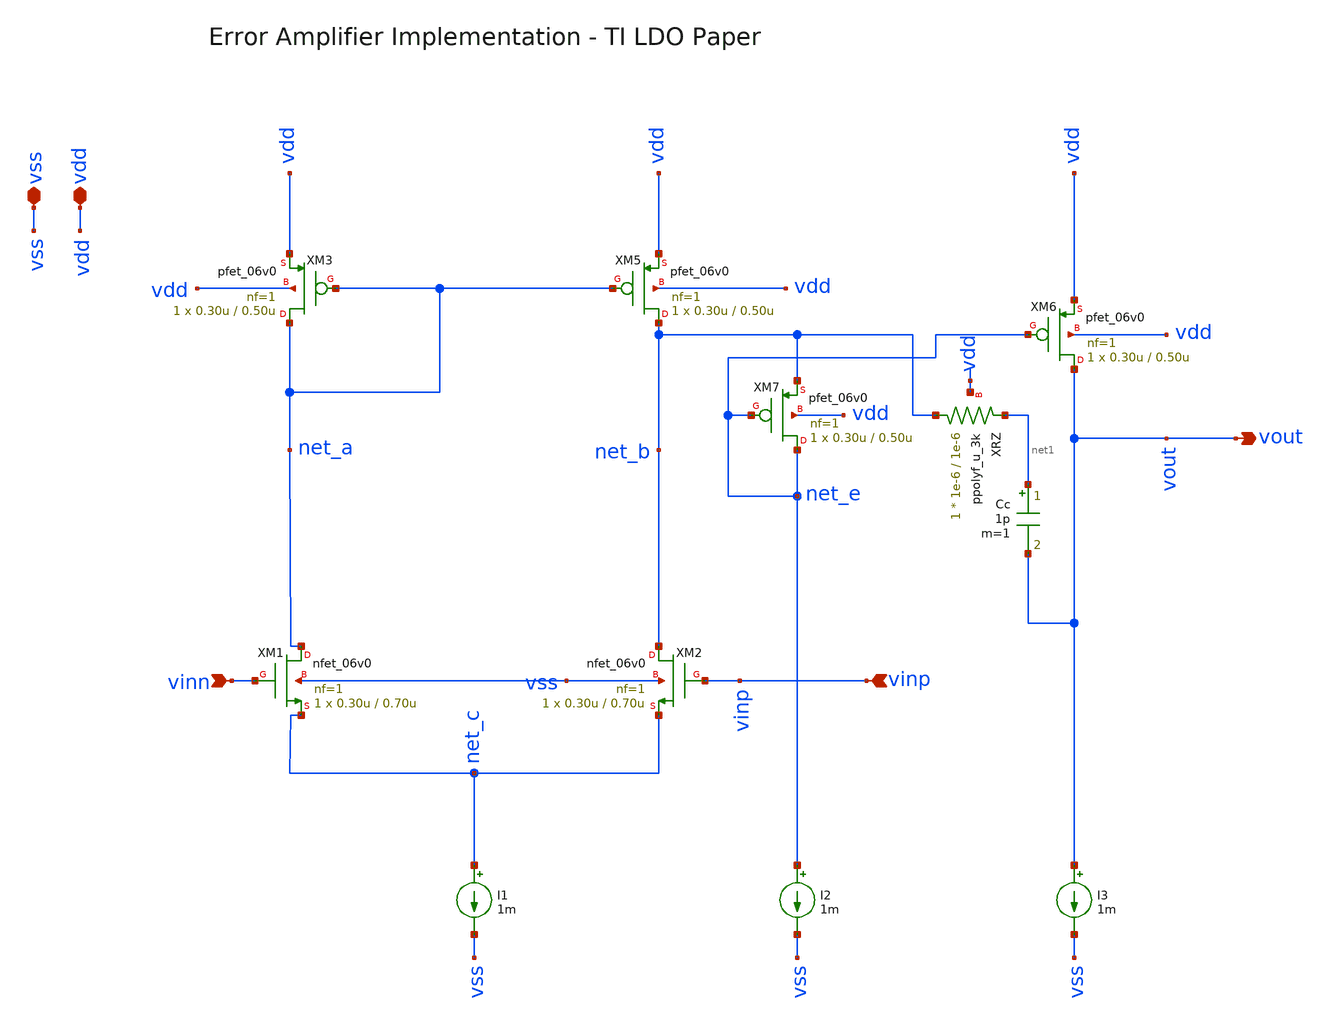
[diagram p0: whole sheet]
** sch_path: analog-db/drawings/ldo-005-ti-ldo-buffer-ref/gf180/error_amp/error_amp_diode_connected.sch
**.subckt error_amp_diode_connected vdd vss vinp vout vinn
*.iopin vdd
*.iopin vss
*.ipin vinp
*.opin vout
*.ipin vinn
XM2 net_b vinp net_c vss nfet_06v0 L=0.70u W=0.30u nf=1 ad='int((nf+1)/2) * W/nf * 0.18u' as='int((nf+2)/2) * W/nf * 0.18u'
+ pd='2*int((nf+1)/2) * (W/nf + 0.18u)' ps='2*int((nf+2)/2) * (W/nf + 0.18u)' nrd='0.18u / W' nrs='0.18u / W'
+ sa=0 sb=0 sd=0 m=1
I1 net_c vss 1m
I2 net_e vss 1m
I3 vout vss 1m
XM3 net_a net_a vdd vdd pfet_06v0 L=0.50u W=0.30u nf=1 ad='int((nf+1)/2) * W/nf * 0.18u' as='int((nf+2)/2) * W/nf * 0.18u'
+ pd='2*int((nf+1)/2) * (W/nf + 0.18u)' ps='2*int((nf+2)/2) * (W/nf + 0.18u)' nrd='0.18u / W' nrs='0.18u / W'
+ sa=0 sb=0 sd=0 m=1
XM5 net_b net_a vdd vdd pfet_06v0 L=0.50u W=0.30u nf=1 ad='int((nf+1)/2) * W/nf * 0.18u' as='int((nf+2)/2) * W/nf * 0.18u'
+ pd='2*int((nf+1)/2) * (W/nf + 0.18u)' ps='2*int((nf+2)/2) * (W/nf + 0.18u)' nrd='0.18u / W' nrs='0.18u / W'
+ sa=0 sb=0 sd=0 m=1
XM6 vout net_e vdd vdd pfet_06v0 L=0.50u W=0.30u nf=1 ad='int((nf+1)/2) * W/nf * 0.18u' as='int((nf+2)/2) * W/nf * 0.18u'
+ pd='2*int((nf+1)/2) * (W/nf + 0.18u)' ps='2*int((nf+2)/2) * (W/nf + 0.18u)' nrd='0.18u / W' nrs='0.18u / W'
+ sa=0 sb=0 sd=0 m=1
XM7 net_e net_e net_b vdd pfet_06v0 L=0.50u W=0.30u nf=1 ad='int((nf+1)/2) * W/nf * 0.18u' as='int((nf+2)/2) * W/nf * 0.18u'
+ pd='2*int((nf+1)/2) * (W/nf + 0.18u)' ps='2*int((nf+2)/2) * (W/nf + 0.18u)' nrd='0.18u / W' nrs='0.18u / W'
+ sa=0 sb=0 sd=0 m=1
Cc net1 vout 1p m=1
XRZ net_b net1 vdd ppolyf_u_3k r_width=1e-6 r_length=1e-6 m=1
XM1 net_a vinn net_c vss nfet_06v0 L=0.70u W=0.30u nf=1 ad='int((nf+1)/2) * W/nf * 0.18u' as='int((nf+2)/2) * W/nf * 0.18u'
+ pd='2*int((nf+1)/2) * (W/nf + 0.18u)' ps='2*int((nf+2)/2) * (W/nf + 0.18u)' nrd='0.18u / W' nrs='0.18u / W'
+ sa=0 sb=0 sd=0 m=1
**.ends
.end
